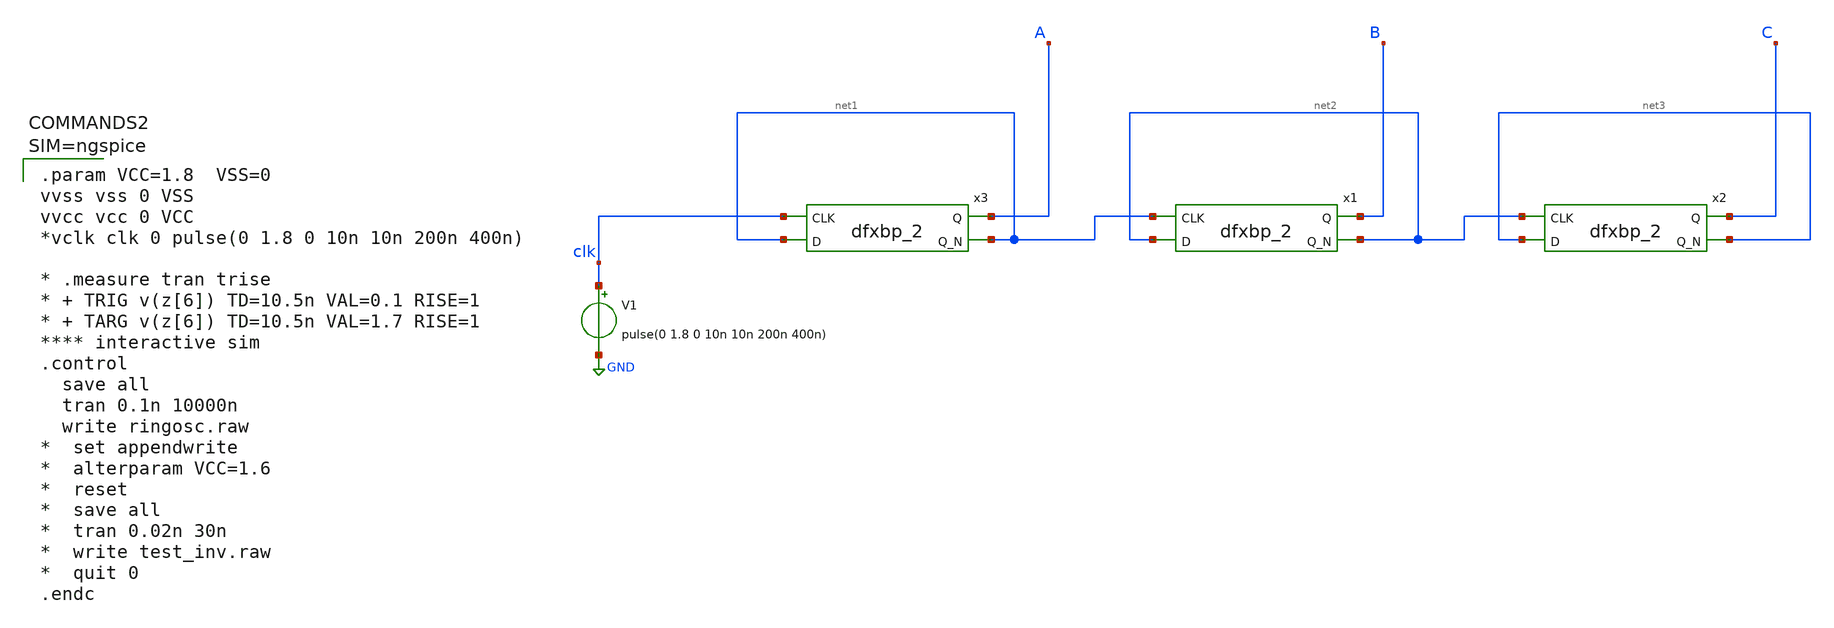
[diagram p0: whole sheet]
** sch_path: xschem/ringosc.sch
.lib $::SKYWATER_MODELS/sky130.lib.spice tt
.include $::SKYWATER_STDCELLS/sky130_fd_sc_hd.spice

**.subckt ringosc
V1 clk GND pulse(0 1.8 0 10n 10n 200n 400n)
x3 clk net1 VSS VSS VCC VCC A net1 sky130_fd_sc_hd__dfxbp_2
x1 net1 net2 VSS VSS VCC VCC B net2 sky130_fd_sc_hd__dfxbp_2
x2 net2 net3 VSS VSS VCC VCC C net3 sky130_fd_sc_hd__dfxbp_2
**** begin user architecture code


.param VCC=1.8  VSS=0
vvss vss 0 VSS
vvcc vcc 0 VCC
*vclk clk 0 pulse(0 1.8 0 10n 10n 200n 400n)

* .measure tran trise
* + TRIG v(z[6]) TD=10.5n VAL=0.1 RISE=1
* + TARG v(z[6]) TD=10.5n VAL=1.7 RISE=1
**** interactive sim
.control
  save all
  tran 0.1n 10000n
  write ringosc.raw
*  set appendwrite
*  alterparam VCC=1.6
*  reset
*  save all
*  tran 0.02n 30n
*  write test_inv.raw
*  quit 0
.endc



**** end user architecture code
**.ends
.GLOBAL GND
.end
